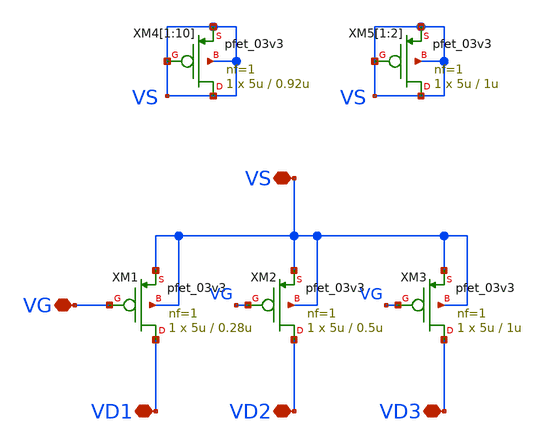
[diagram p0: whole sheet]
** sch_path: Current_Source/pmos_char.sch
**.subckt pmos_char VD1 VD2 VD3 VG VS
*.iopin VD1
*.iopin VD2
*.iopin VD3
*.iopin VG
*.iopin VS
XM1 VD1 VG VS VS pfet_03v3 L=0.28u W=5u nf=1 ad='int((nf+1)/2) * W/nf * 0.18u' as='int((nf+2)/2) * W/nf * 0.18u'
+ pd='2*int((nf+1)/2) * (W/nf + 0.18u)' ps='2*int((nf+2)/2) * (W/nf + 0.18u)' nrd='0.18u / W' nrs='0.18u / W'
+ sa=0 sb=0 sd=0 m=1
XM2 VD2 VG VS VS pfet_03v3 L=0.5u W=5u nf=1 ad='int((nf+1)/2) * W/nf * 0.18u' as='int((nf+2)/2) * W/nf * 0.18u'
+ pd='2*int((nf+1)/2) * (W/nf + 0.18u)' ps='2*int((nf+2)/2) * (W/nf + 0.18u)' nrd='0.18u / W' nrs='0.18u / W'
+ sa=0 sb=0 sd=0 m=1
XM3 VD3 VG VS VS pfet_03v3 L=1u W=5u nf=1 ad='int((nf+1)/2) * W/nf * 0.18u' as='int((nf+2)/2) * W/nf * 0.18u'
+ pd='2*int((nf+1)/2) * (W/nf + 0.18u)' ps='2*int((nf+2)/2) * (W/nf + 0.18u)' nrd='0.18u / W' nrs='0.18u / W'
+ sa=0 sb=0 sd=0 m=1
XM4[1] VS VS VS VS pfet_03v3 L=0.92u W=5u nf=1 ad='int((nf+1)/2) * W/nf * 0.18u' as='int((nf+2)/2) * W/nf * 0.18u'
+ pd='2*int((nf+1)/2) * (W/nf + 0.18u)' ps='2*int((nf+2)/2) * (W/nf + 0.18u)' nrd='0.18u / W' nrs='0.18u / W'
+ sa=0 sb=0 sd=0 m=1
XM4[2] VS VS VS VS pfet_03v3 L=0.92u W=5u nf=1 ad='int((nf+1)/2) * W/nf * 0.18u' as='int((nf+2)/2) * W/nf * 0.18u'
+ pd='2*int((nf+1)/2) * (W/nf + 0.18u)' ps='2*int((nf+2)/2) * (W/nf + 0.18u)' nrd='0.18u / W' nrs='0.18u / W'
+ sa=0 sb=0 sd=0 m=1
XM4[3] VS VS VS VS pfet_03v3 L=0.92u W=5u nf=1 ad='int((nf+1)/2) * W/nf * 0.18u' as='int((nf+2)/2) * W/nf * 0.18u'
+ pd='2*int((nf+1)/2) * (W/nf + 0.18u)' ps='2*int((nf+2)/2) * (W/nf + 0.18u)' nrd='0.18u / W' nrs='0.18u / W'
+ sa=0 sb=0 sd=0 m=1
XM4[4] VS VS VS VS pfet_03v3 L=0.92u W=5u nf=1 ad='int((nf+1)/2) * W/nf * 0.18u' as='int((nf+2)/2) * W/nf * 0.18u'
+ pd='2*int((nf+1)/2) * (W/nf + 0.18u)' ps='2*int((nf+2)/2) * (W/nf + 0.18u)' nrd='0.18u / W' nrs='0.18u / W'
+ sa=0 sb=0 sd=0 m=1
XM4[5] VS VS VS VS pfet_03v3 L=0.92u W=5u nf=1 ad='int((nf+1)/2) * W/nf * 0.18u' as='int((nf+2)/2) * W/nf * 0.18u'
+ pd='2*int((nf+1)/2) * (W/nf + 0.18u)' ps='2*int((nf+2)/2) * (W/nf + 0.18u)' nrd='0.18u / W' nrs='0.18u / W'
+ sa=0 sb=0 sd=0 m=1
XM4[6] VS VS VS VS pfet_03v3 L=0.92u W=5u nf=1 ad='int((nf+1)/2) * W/nf * 0.18u' as='int((nf+2)/2) * W/nf * 0.18u'
+ pd='2*int((nf+1)/2) * (W/nf + 0.18u)' ps='2*int((nf+2)/2) * (W/nf + 0.18u)' nrd='0.18u / W' nrs='0.18u / W'
+ sa=0 sb=0 sd=0 m=1
XM4[7] VS VS VS VS pfet_03v3 L=0.92u W=5u nf=1 ad='int((nf+1)/2) * W/nf * 0.18u' as='int((nf+2)/2) * W/nf * 0.18u'
+ pd='2*int((nf+1)/2) * (W/nf + 0.18u)' ps='2*int((nf+2)/2) * (W/nf + 0.18u)' nrd='0.18u / W' nrs='0.18u / W'
+ sa=0 sb=0 sd=0 m=1
XM4[8] VS VS VS VS pfet_03v3 L=0.92u W=5u nf=1 ad='int((nf+1)/2) * W/nf * 0.18u' as='int((nf+2)/2) * W/nf * 0.18u'
+ pd='2*int((nf+1)/2) * (W/nf + 0.18u)' ps='2*int((nf+2)/2) * (W/nf + 0.18u)' nrd='0.18u / W' nrs='0.18u / W'
+ sa=0 sb=0 sd=0 m=1
XM4[9] VS VS VS VS pfet_03v3 L=0.92u W=5u nf=1 ad='int((nf+1)/2) * W/nf * 0.18u' as='int((nf+2)/2) * W/nf * 0.18u'
+ pd='2*int((nf+1)/2) * (W/nf + 0.18u)' ps='2*int((nf+2)/2) * (W/nf + 0.18u)' nrd='0.18u / W' nrs='0.18u / W'
+ sa=0 sb=0 sd=0 m=1
XM4[10] VS VS VS VS pfet_03v3 L=0.92u W=5u nf=1 ad='int((nf+1)/2) * W/nf * 0.18u' as='int((nf+2)/2) * W/nf * 0.18u'
+ pd='2*int((nf+1)/2) * (W/nf + 0.18u)' ps='2*int((nf+2)/2) * (W/nf + 0.18u)' nrd='0.18u / W' nrs='0.18u / W'
+ sa=0 sb=0 sd=0 m=1
XM5[1] VS VS VS VS pfet_03v3 L=1u W=5u nf=1 ad='int((nf+1)/2) * W/nf * 0.18u' as='int((nf+2)/2) * W/nf * 0.18u'
+ pd='2*int((nf+1)/2) * (W/nf + 0.18u)' ps='2*int((nf+2)/2) * (W/nf + 0.18u)' nrd='0.18u / W' nrs='0.18u / W'
+ sa=0 sb=0 sd=0 m=1
XM5[2] VS VS VS VS pfet_03v3 L=1u W=5u nf=1 ad='int((nf+1)/2) * W/nf * 0.18u' as='int((nf+2)/2) * W/nf * 0.18u'
+ pd='2*int((nf+1)/2) * (W/nf + 0.18u)' ps='2*int((nf+2)/2) * (W/nf + 0.18u)' nrd='0.18u / W' nrs='0.18u / W'
+ sa=0 sb=0 sd=0 m=1
**.ends
.end
